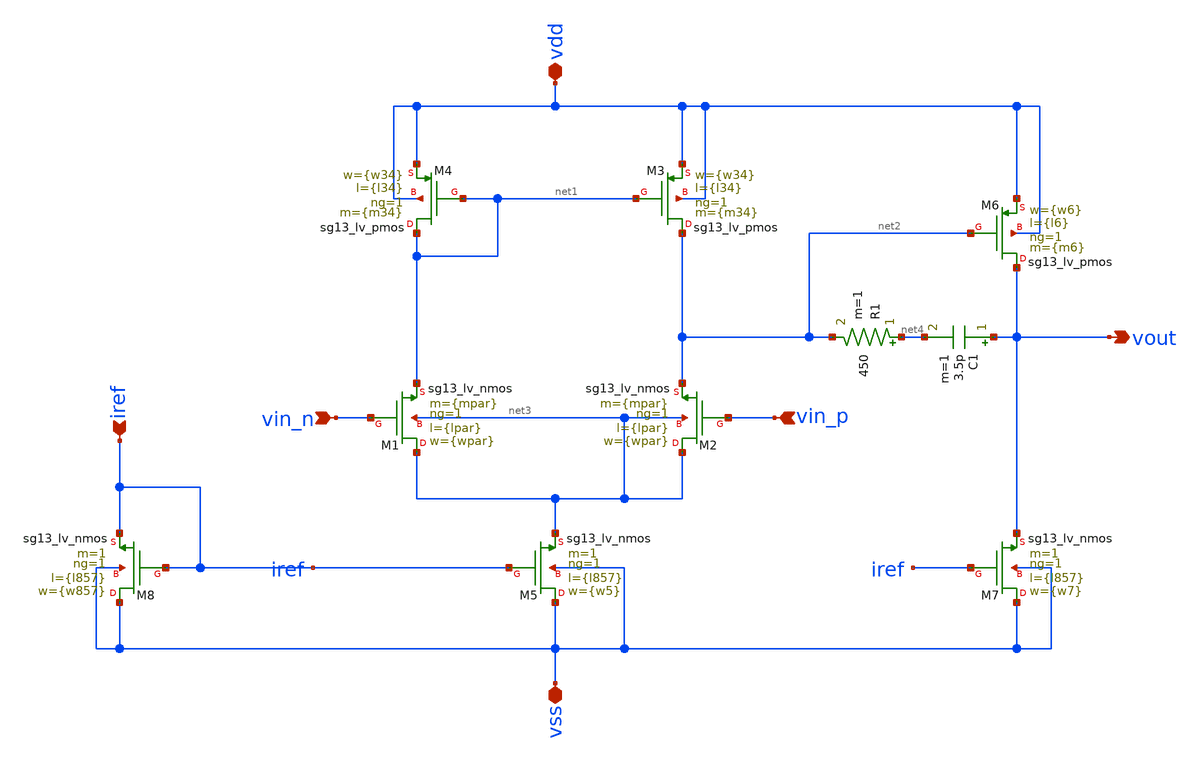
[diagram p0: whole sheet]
** sch_path: ihp_ota_v2.sch
**.subckt ihp_ota_v2 iref vin_n vin_p vdd vss vout
*.ipin iref
*.ipin vin_n
*.ipin vin_p
*.iopin vdd
*.iopin vss
*.opin vout
XM1 net3 vin_n net1 net3 sg13_lv_nmos w={wpar} l={lpar} ng=1 m={mpar} mm_ok=1
XM2 net3 vin_p net2 net3 sg13_lv_nmos w={wpar} l={lpar} ng=1 m={mpar} mm_ok=1
XM3 net2 net1 vdd vdd sg13_lv_pmos w={w34} l={l34} ng=1 m={m34} mm_ok=1
XM4 net1 net1 vdd vdd sg13_lv_pmos w={w34} l={l34} ng=1 m={m34} mm_ok=1
XM5 vss iref net3 vss sg13_lv_nmos w={w5} l={l857} ng=1 m=1 mm_ok=1
XM6 vout net2 vdd vdd sg13_lv_pmos w={w6} l={l6} ng=1 m={m6} mm_ok=1
XM7 vss iref vout vss sg13_lv_nmos w={w7} l={l857} ng=1 m=1 mm_ok=1
XM8 vss iref iref vss sg13_lv_nmos w={w857} l={l857} ng=1 m=1 mm_ok=1
C1 vout net4 3.5p m=1
R1 net4 net2 450 m=1
**.ends
.end
